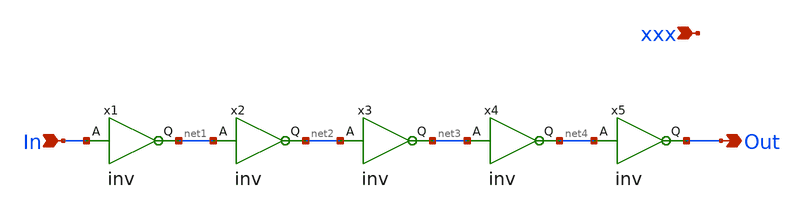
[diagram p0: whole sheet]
** sch_path: schemas/RING_OSC.sch
**.subckt RING_OSC Out In xxx
*.opin Out
*.ipin In
*.ipin xxx
x1 net1 In inv
x2 net2 net1 inv
x3 net3 net2 inv
x4 net4 net3 inv
x5 Out net4 inv
**.ends

* expanding   symbol:  /home/mstopyra/Documents/FINAL/inv.sym # of pins=2
** sym_path: schemas/inv.sym
** sch_path: schemas/inv.sch
.subckt inv Q A
*.ipin A
*.opin Q
XM1 Q A GND GND sky130_fd_pr__nfet_01v8 L=0.15 W=1 nf=1 ad='int((nf+1)/2) * W/nf * 0.29' as='int((nf+2)/2) * W/nf * 0.29'
+ pd='2*int((nf+1)/2) * (W/nf + 0.29)' ps='2*int((nf+2)/2) * (W/nf + 0.29)' nrd='0.29 / W' nrs='0.29 / W'
+ sa=0 sb=0 sd=0 mult=1 m=1
XM2 Q A VDD VDD sky130_fd_pr__pfet_01v8 L=0.15 W=1 nf=1 ad='int((nf+1)/2) * W/nf * 0.29' as='int((nf+2)/2) * W/nf * 0.29'
+ pd='2*int((nf+1)/2) * (W/nf + 0.29)' ps='2*int((nf+2)/2) * (W/nf + 0.29)' nrd='0.29 / W' nrs='0.29 / W'
+ sa=0 sb=0 sd=0 mult=1 m=1
.ends

.GLOBAL VDD
.GLOBAL GND
.end
